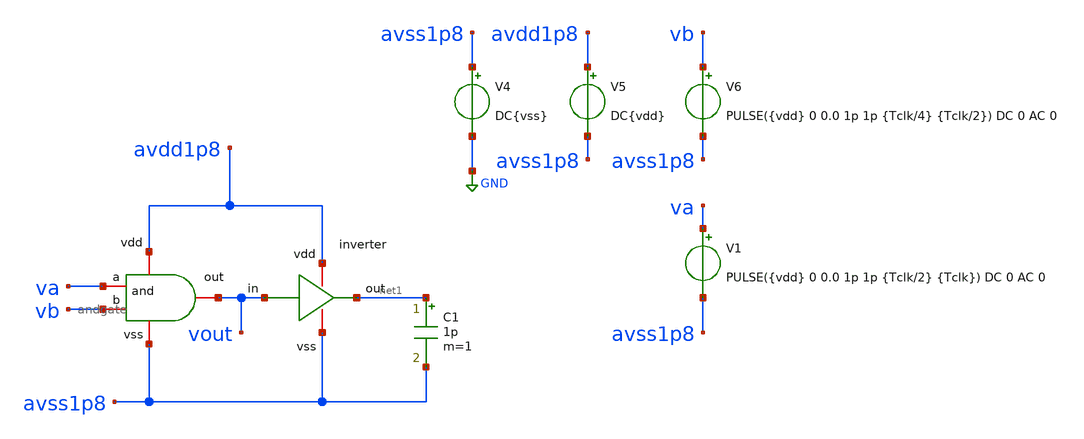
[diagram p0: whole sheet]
** sch_path: verification/testbenches/tb_andgate.sch
**.subckt tb_andgate
C1 net1 avss1p8 1p m=1
V4 avss1p8 GND DC{vss}
V5 avdd1p8 avss1p8 DC{vdd}
V6 vb avss1p8 PULSE({vdd} 0 0.0 1p 1p {Tclk/4} {Tclk/2}) DC 0 AC 0
x2 avdd1p8 net1 vout avss1p8 inverter
V1 va avss1p8 PULSE({vdd} 0 0.0 1p 1p {Tclk/2} {Tclk}) DC 0 AC 0
x1 avdd1p8 va vb vout avss1p8 andgate
**** begin user architecture code


* Circuit Parameters
.param vdd = 1.2
.param vss = 0.0
.param Tclk = 10n
.options TEMP = 27.0
* Include Models - IHP SG13G2
.lib cornerMOSlv.lib mos_tt
* OP Parameters & Singals to save
.save all
*Simulations
.control
tran 0.01u 100n
setplot tran1
plot v(va) v(vb) + 1.2 v(vout) + 2.4
set filetype = ascii
write dcsweep.raw
.endc
.end


**** end user architecture code
**.ends

* expanding   symbol:  blocks/inverter/schematic/inverter.sym # of pins=4
** sym_path: design/blocks/inverter/schematic/inverter.sym
** sch_path: design/blocks/inverter/schematic/inverter.sch
.subckt inverter vdd out in vss
*.iopin vdd
*.iopin out
*.iopin vss
*.iopin in
XM1 out in vss vss sky130_fd_pr__nfet_01v8 L=0.15 W=0.75 nf=1 ad='int((nf+1)/2) * W/nf * 0.29' as='int((nf+2)/2) * W/nf * 0.29'
+ pd='2*int((nf+1)/2) * (W/nf + 0.29)' ps='2*int((nf+2)/2) * (W/nf + 0.29)' nrd='0.29 / W' nrs='0.29 / W'
+ sa=0 sb=0 sd=0 mult=1 m=1
XM2 out in vdd vdd sky130_fd_pr__pfet_01v8 L=0.15 W=1.5 nf=1 ad='int((nf+1)/2) * W/nf * 0.29' as='int((nf+2)/2) * W/nf * 0.29'
+ pd='2*int((nf+1)/2) * (W/nf + 0.29)' ps='2*int((nf+2)/2) * (W/nf + 0.29)' nrd='0.29 / W' nrs='0.29 / W'
+ sa=0 sb=0 sd=0 mult=1 m=1
.ends


* expanding   symbol:  blocks/andgate/schematic/andgate.sym # of pins=5
** sym_path: design/blocks/andgate/schematic/andgate.sym
** sch_path: design/blocks/andgate/schematic/andgate.sch
.subckt andgate vdd a b out vss
*.iopin b
*.iopin a
*.iopin vdd
*.iopin vss
*.iopin out
XM1 net1 b vss vss sg13_lv_nmos w=1.5u l=0.15u ng=1 m=1 mm_ok=1
XM4 net2 a vdd vdd sg13_lv_pmos w=1.5u l=0.15u ng=1 m=1 mm_ok=1
x1 vdd out net2 vss inverter
XM3 net2 a net1 vss sg13_lv_nmos w=1.5u l=0.15u ng=1 m=1 mm_ok=1
XM5 net2 b vdd vdd sg13_lv_pmos w=1.5u l=0.15u ng=1 m=1 mm_ok=1
.ends

.GLOBAL GND
.end
